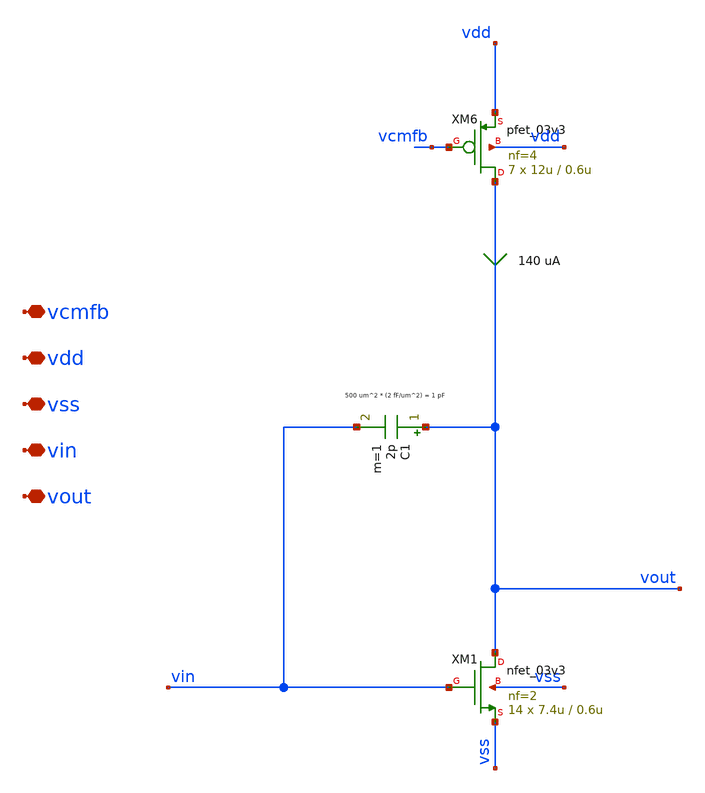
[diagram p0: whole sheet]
** sch_path: xschem/archive/ota/s2_half_circuit.sch
**.subckt s2_half_circuit vcmfb vdd vss vin vout
*.iopin vcmfb
*.iopin vdd
*.iopin vss
*.iopin vin
*.iopin vout
XM6 vout vcmfb vdd vdd pfet_03v3 L=0.6u W=12u nf=4 ad='int((nf+1)/2) * W/nf * 0.18u' as='int((nf+2)/2) * W/nf * 0.18u'
+ pd='2*int((nf+1)/2) * (W/nf + 0.18u)' ps='2*int((nf+2)/2) * (W/nf + 0.18u)' nrd='0.18u / W' nrs='0.18u / W'
+ sa=0 sb=0 sd=0 m=7
XM1 vout vin vss vss nfet_03v3 L=0.6u W=7.4u nf=2 ad='int((nf+1)/2) * W/nf * 0.18u' as='int((nf+2)/2) * W/nf * 0.18u'
+ pd='2*int((nf+1)/2) * (W/nf + 0.18u)' ps='2*int((nf+2)/2) * (W/nf + 0.18u)' nrd='0.18u / W' nrs='0.18u / W'
+ sa=0 sb=0 sd=0 m=14
C1 vout vin 2p m=1
**.ends
.end
